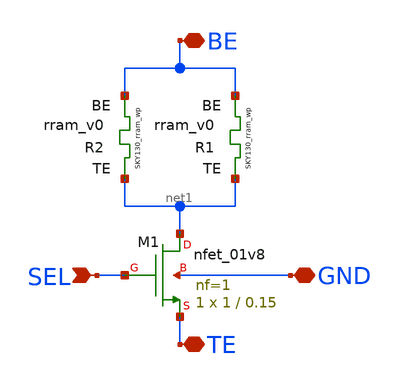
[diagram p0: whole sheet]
** sch_path: Ricardo/1T2R/1T2R.sch
**.subckt 1T2R BE TE GND SEL
*.iopin BE
*.iopin TE
*.iopin GND
*.ipin SEL
XR1 net1 BE rram_v0
XR2 net1 BE rram_v0
XM1 net1 SEL TE GND sky130_fd_pr__nfet_01v8 L=0.15 W=1 nf=1 ad='int((nf+1)/2) * W/nf * 0.29' as='int((nf+2)/2) * W/nf * 0.29'
+ pd='2*int((nf+1)/2) * (W/nf + 0.29)' ps='2*int((nf+2)/2) * (W/nf + 0.29)' nrd='0.29 / W' nrs='0.29 / W'
+ sa=0 sb=0 sd=0 mult=1 m=1
**.ends
.end
